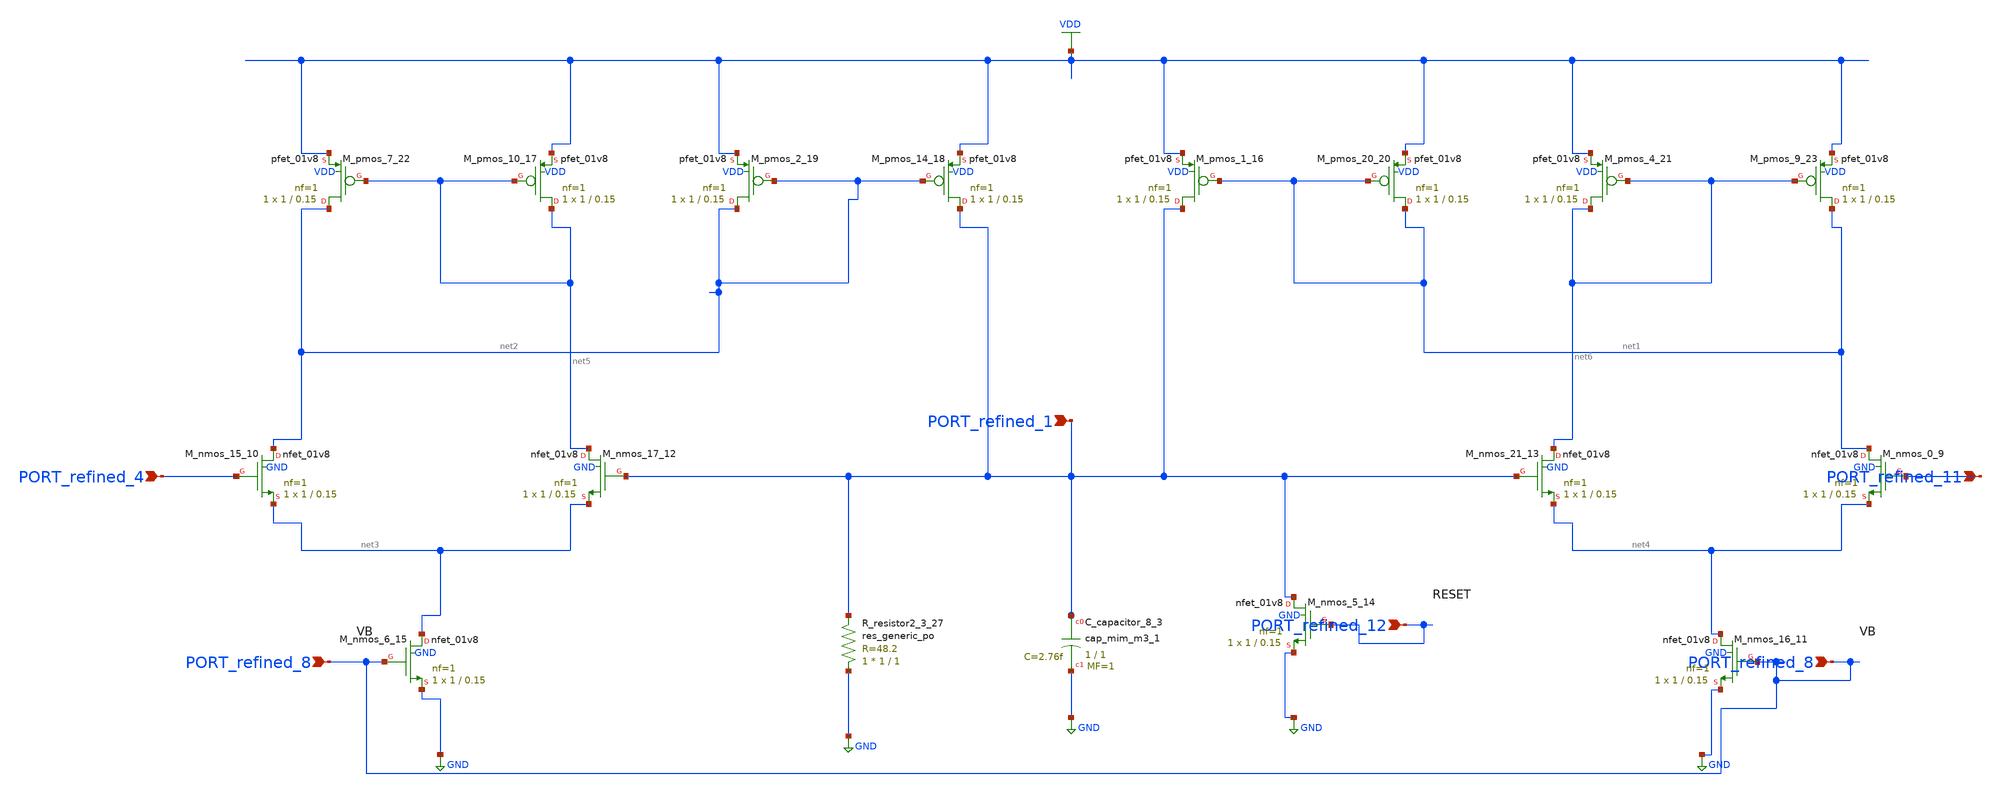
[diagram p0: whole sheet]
** sch_path: schematics/10_1109_ACCESS_2020_2989192_09_004.sch
**.subckt 10_1109_ACCESS_2020_2989192_09_004 PORT_refined_12 PORT_refined_8 PORT_refined_8
*+ PORT_refined_4 PORT_refined_1 PORT_refined_11
*.ipin PORT_refined_12
*.ipin PORT_refined_8
*.ipin PORT_refined_8
*.ipin PORT_refined_4
*.ipin PORT_refined_1
*.ipin PORT_refined_11
XC_capacitor_8_3 PORT_refined_1 GND sky130_fd_pr__cap_mim_m3_1 W=1 L=1 MF=1 m=1
XM_nmos_0_9 net1 PORT_refined_11 net4 GND sky130_fd_pr__nfet_01v8 L=0.15 W=1 nf=1 ad='int((1 + 1)/2) * 1 / 1 * 0.29'
+ as='int((1 + 2)/2) * 1 / 1 * 0.29' pd='2*int((1 + 1)/2) * (1 / 1 + 0.29)' ps='2*int((1 + 2)/2) * (1 / 1 + 0.29)'
+ nrd='0.29 / 1 ' nrs='0.29 / 1 ' sa=0 sb=0 sd=0 mult=1 m=1
XM_nmos_15_10 net2 PORT_refined_4 net3 GND sky130_fd_pr__nfet_01v8 L=0.15 W=1 nf=1 ad='int((1 + 1)/2) * 1 / 1 * 0.29'
+ as='int((1 + 2)/2) * 1 / 1 * 0.29' pd='2*int((1 + 1)/2) * (1 / 1 + 0.29)' ps='2*int((1 + 2)/2) * (1 / 1 + 0.29)'
+ nrd='0.29 / 1 ' nrs='0.29 / 1 ' sa=0 sb=0 sd=0 mult=1 m=1
XM_nmos_16_11 net4 PORT_refined_8 GND GND sky130_fd_pr__nfet_01v8 L=0.15 W=1 nf=1 ad='int((1 + 1)/2) * 1 / 1 * 0.29'
+ as='int((1 + 2)/2) * 1 / 1 * 0.29' pd='2*int((1 + 1)/2) * (1 / 1 + 0.29)' ps='2*int((1 + 2)/2) * (1 / 1 + 0.29)'
+ nrd='0.29 / 1 ' nrs='0.29 / 1 ' sa=0 sb=0 sd=0 mult=1 m=1
XM_nmos_17_12 net5 PORT_refined_1 net3 GND sky130_fd_pr__nfet_01v8 L=0.15 W=1 nf=1 ad='int((1 + 1)/2) * 1 / 1 * 0.29'
+ as='int((1 + 2)/2) * 1 / 1 * 0.29' pd='2*int((1 + 1)/2) * (1 / 1 + 0.29)' ps='2*int((1 + 2)/2) * (1 / 1 + 0.29)'
+ nrd='0.29 / 1 ' nrs='0.29 / 1 ' sa=0 sb=0 sd=0 mult=1 m=1
XM_nmos_21_13 net6 PORT_refined_1 net4 GND sky130_fd_pr__nfet_01v8 L=0.15 W=1 nf=1 ad='int((1 + 1)/2) * 1 / 1 * 0.29'
+ as='int((1 + 2)/2) * 1 / 1 * 0.29' pd='2*int((1 + 1)/2) * (1 / 1 + 0.29)' ps='2*int((1 + 2)/2) * (1 / 1 + 0.29)'
+ nrd='0.29 / 1 ' nrs='0.29 / 1 ' sa=0 sb=0 sd=0 mult=1 m=1
XM_nmos_5_14 PORT_refined_1 PORT_refined_12 GND GND sky130_fd_pr__nfet_01v8 L=0.15 W=1 nf=1 ad='int((1 + 1)/2) * 1 / 1 * 0.29'
+ as='int((1 + 2)/2) * 1 / 1 * 0.29' pd='2*int((1 + 1)/2) * (1 / 1 + 0.29)' ps='2*int((1 + 2)/2) * (1 / 1 + 0.29)'
+ nrd='0.29 / 1 ' nrs='0.29 / 1 ' sa=0 sb=0 sd=0 mult=1 m=1
XM_nmos_6_15 net3 PORT_refined_8 GND GND sky130_fd_pr__nfet_01v8 L=0.15 W=1 nf=1 ad='int((1 + 1)/2) * 1 / 1 * 0.29'
+ as='int((1 + 2)/2) * 1 / 1 * 0.29' pd='2*int((1 + 1)/2) * (1 / 1 + 0.29)' ps='2*int((1 + 2)/2) * (1 / 1 + 0.29)'
+ nrd='0.29 / 1 ' nrs='0.29 / 1 ' sa=0 sb=0 sd=0 mult=1 m=1
XM_pmos_1_16 PORT_refined_1 net1 VDD VDD sky130_fd_pr__pfet_01v8 L=0.15 W=1 nf=1 ad='int((1 + 1)/2) * 1 / 1 * 0.29'
+ as='int((1 + 2)/2) * 1 / 1 * 0.29' pd='2*int((1 + 1)/2) * (1 / 1 + 0.29)' ps='2*int((1 + 2)/2) * (1 / 1 + 0.29)'
+ nrd='0.29 / 1 ' nrs='0.29 / 1 ' sa=0 sb=0 sd=0 mult=1 m=1
XM_pmos_10_17 net5 net5 VDD VDD sky130_fd_pr__pfet_01v8 L=0.15 W=1 nf=1 ad='int((1 + 1)/2) * 1 / 1 * 0.29'
+ as='int((1 + 2)/2) * 1 / 1 * 0.29' pd='2*int((1 + 1)/2) * (1 / 1 + 0.29)' ps='2*int((1 + 2)/2) * (1 / 1 + 0.29)'
+ nrd='0.29 / 1 ' nrs='0.29 / 1 ' sa=0 sb=0 sd=0 mult=1 m=1
XM_pmos_14_18 PORT_refined_1 net2 VDD VDD sky130_fd_pr__pfet_01v8 L=0.15 W=1 nf=1 ad='int((1 + 1)/2) * 1 / 1 * 0.29'
+ as='int((1 + 2)/2) * 1 / 1 * 0.29' pd='2*int((1 + 1)/2) * (1 / 1 + 0.29)' ps='2*int((1 + 2)/2) * (1 / 1 + 0.29)'
+ nrd='0.29 / 1 ' nrs='0.29 / 1 ' sa=0 sb=0 sd=0 mult=1 m=1
XM_pmos_2_19 net2 net2 VDD VDD sky130_fd_pr__pfet_01v8 L=0.15 W=1 nf=1 ad='int((1 + 1)/2) * 1 / 1 * 0.29'
+ as='int((1 + 2)/2) * 1 / 1 * 0.29' pd='2*int((1 + 1)/2) * (1 / 1 + 0.29)' ps='2*int((1 + 2)/2) * (1 / 1 + 0.29)'
+ nrd='0.29 / 1 ' nrs='0.29 / 1 ' sa=0 sb=0 sd=0 mult=1 m=1
XM_pmos_20_20 net1 net1 VDD VDD sky130_fd_pr__pfet_01v8 L=0.15 W=1 nf=1 ad='int((1 + 1)/2) * 1 / 1 * 0.29'
+ as='int((1 + 2)/2) * 1 / 1 * 0.29' pd='2*int((1 + 1)/2) * (1 / 1 + 0.29)' ps='2*int((1 + 2)/2) * (1 / 1 + 0.29)'
+ nrd='0.29 / 1 ' nrs='0.29 / 1 ' sa=0 sb=0 sd=0 mult=1 m=1
XM_pmos_4_21 net6 net6 VDD VDD sky130_fd_pr__pfet_01v8 L=0.15 W=1 nf=1 ad='int((1 + 1)/2) * 1 / 1 * 0.29'
+ as='int((1 + 2)/2) * 1 / 1 * 0.29' pd='2*int((1 + 1)/2) * (1 / 1 + 0.29)' ps='2*int((1 + 2)/2) * (1 / 1 + 0.29)'
+ nrd='0.29 / 1 ' nrs='0.29 / 1 ' sa=0 sb=0 sd=0 mult=1 m=1
XM_pmos_7_22 net2 net5 VDD VDD sky130_fd_pr__pfet_01v8 L=0.15 W=1 nf=1 ad='int((1 + 1)/2) * 1 / 1 * 0.29'
+ as='int((1 + 2)/2) * 1 / 1 * 0.29' pd='2*int((1 + 1)/2) * (1 / 1 + 0.29)' ps='2*int((1 + 2)/2) * (1 / 1 + 0.29)'
+ nrd='0.29 / 1 ' nrs='0.29 / 1 ' sa=0 sb=0 sd=0 mult=1 m=1
XM_pmos_9_23 net1 net6 VDD VDD sky130_fd_pr__pfet_01v8 L=0.15 W=1 nf=1 ad='int((1 + 1)/2) * 1 / 1 * 0.29'
+ as='int((1 + 2)/2) * 1 / 1 * 0.29' pd='2*int((1 + 1)/2) * (1 / 1 + 0.29)' ps='2*int((1 + 2)/2) * (1 / 1 + 0.29)'
+ nrd='0.29 / 1 ' nrs='0.29 / 1 ' sa=0 sb=0 sd=0 mult=1 m=1
XR_resistor2_3_27 GND PORT_refined_1 sky130_fd_pr__res_generic_po W=1 L=1 m=1
**.ends
.GLOBAL GND
.GLOBAL VDD
.end
